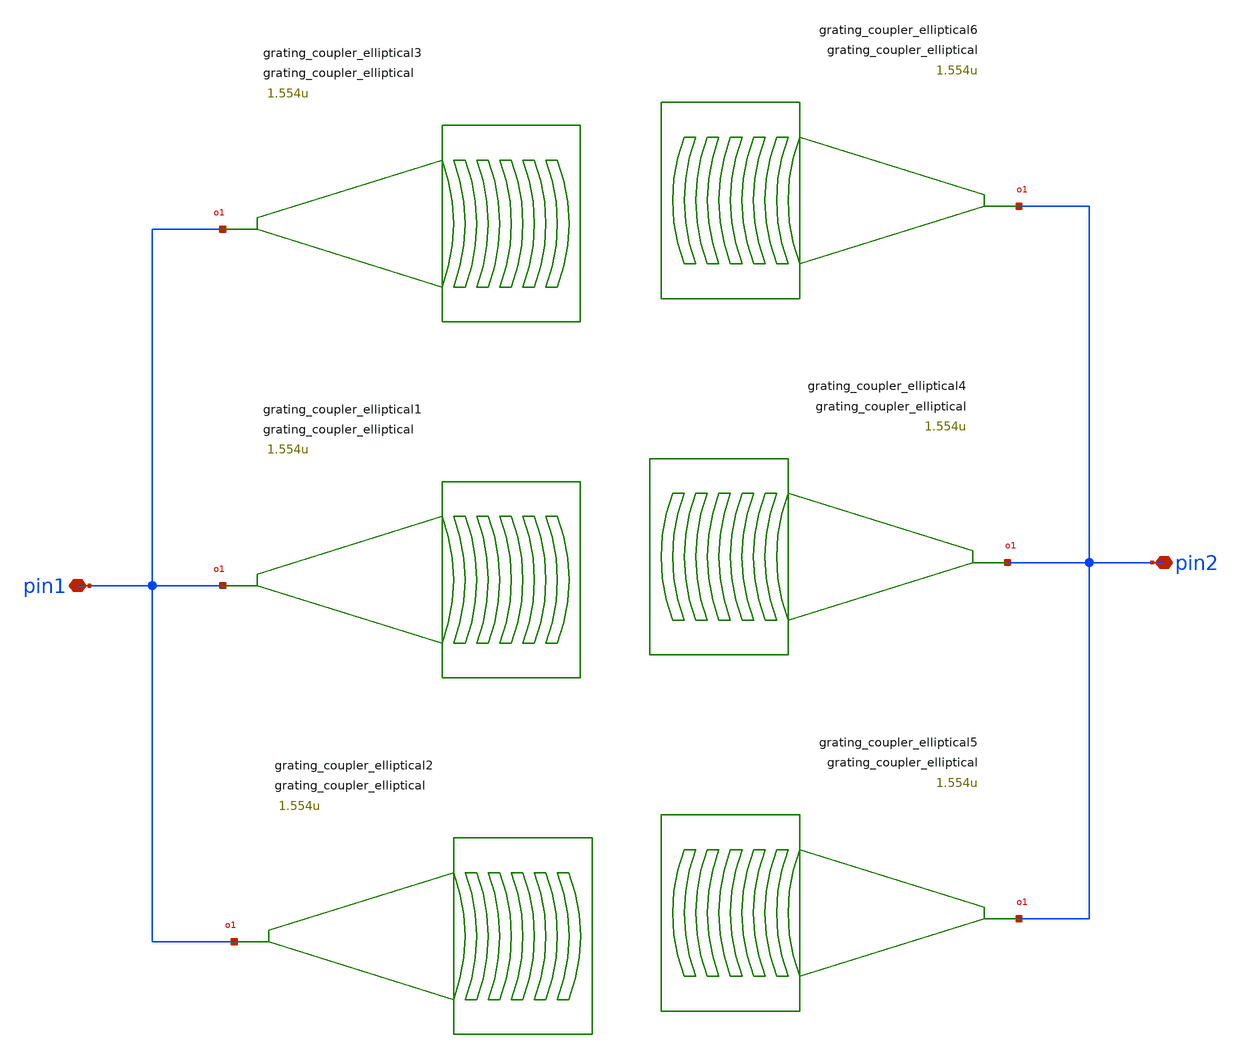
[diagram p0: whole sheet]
** sch_path: xschem/tests/test_sch/test_grating_coupler_elliptical.sch
* Copyright (c) 2024, Mabrains LLC
* Licensed under the GNU Lesser General Public License, Version 3.0 (the "License");
* you may not use this file except in compliance with the License.
* GNU Lesser General Public License
* Version 3, 29 June 2007
* This program is free software: you can redistribute it and/or modify
* it under the terms of the GNU Lesser General Public License as published
* by the Free Software Foundation, either version 3 of the License, or
* (at your option) any later version.
* This program is distributed in the hope that it will be useful,
* but WITHOUT ANY WARRANTY; without even the implied warranty of
* MERCHANTABILITY or FITNESS FOR A PARTICULAR PURPOSE.  See the
* GNU Lesser General Public License for more details.
* You should have received a copy of the GNU Lesser General Public License
* along with this program.  If not, see <https://www.gnu.org/licenses/>.
* SPDX-License-Identifier: LGPL-3.0
**.subckt test_grating_coupler_elliptical pin1 pin2
*.iopin pin1
*.iopin pin2
Pgrating_coupler_elliptical1 pin1 grating_coupler_elliptical taper_length=16.6u taper_angle=40.0
+ wavelength=1.554u fiber_angle=15.0 grating_line_width=0.343u n_periods=30 slab_xmin=-1.0u slab_offset=2.0u
Pgrating_coupler_elliptical2 pin1 grating_coupler_elliptical taper_length=16.6u taper_angle=40.0
+ wavelength=1.554u fiber_angle=15.0 grating_line_width=0.343u n_periods=30 slab_xmin=-1.0u slab_offset=2.0u
Pgrating_coupler_elliptical3 pin1 grating_coupler_elliptical taper_length=16.6u taper_angle=40.0
+ wavelength=1.554u fiber_angle=15.0 grating_line_width=0.343u n_periods=30 slab_xmin=-1.0u slab_offset=2.0u
Pgrating_coupler_elliptical4 pin2 grating_coupler_elliptical taper_length=16.6u taper_angle=40.0
+ wavelength=1.554u fiber_angle=15.0 grating_line_width=0.343u n_periods=30 slab_xmin=-1.0u slab_offset=2.0u
Pgrating_coupler_elliptical5 pin2 grating_coupler_elliptical taper_length=16.6u taper_angle=40.0
+ wavelength=1.554u fiber_angle=15.0 grating_line_width=0.343u n_periods=30 slab_xmin=-1.0u slab_offset=2.0u
Pgrating_coupler_elliptical6 pin2 grating_coupler_elliptical taper_length=16.6u taper_angle=40.0
+ wavelength=1.554u fiber_angle=15.0 grating_line_width=0.343u n_periods=30 slab_xmin=-1.0u slab_offset=2.0u
**.ends
.end
